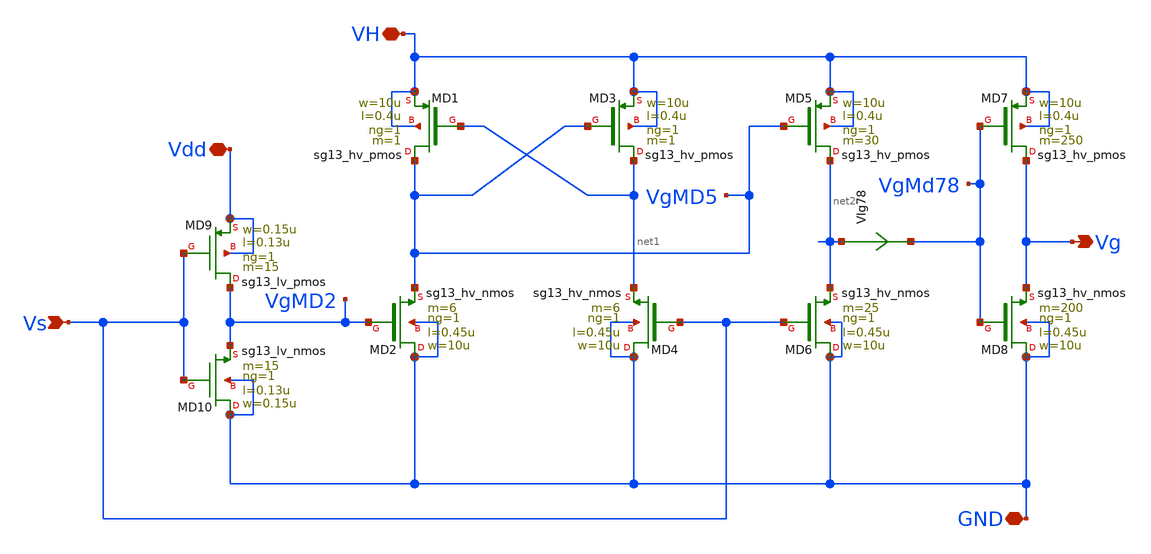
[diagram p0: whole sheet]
** sch_path: ChipUSM_AnalogTrack24/GD/GateDriverV2.sch
**.subckt GateDriverV2 VH Vdd Vs Vg GND
*.iopin VH
*.iopin Vdd
*.ipin Vs
*.opin Vg
*.iopin GND
XMD9 VgMD2 Vs Vdd Vdd sg13_lv_pmos w=0.15u l=0.13u ng=1 m=15 mm_ok=1
XMD10 GND Vs VgMD2 GND sg13_lv_nmos w=0.15u l=0.13u ng=1 m=15 mm_ok=1
XMD1 VgMD5 net1 VH VH sg13_hv_pmos w=10u l=0.4u ng=1 m=1 mm_ok=1
XMD3 net1 VgMD5 VH VH sg13_hv_pmos w=10u l=0.4u ng=1 m=1 mm_ok=1
XMD5 net2 VgMD5 VH VH sg13_hv_pmos w=10u l=0.4u ng=1 m=30 mm_ok=1
XMD7 Vg VgMd78 VH VH sg13_hv_pmos w=10u l=0.4u ng=1 m=250 mm_ok=1
XMD2 GND VgMD2 VgMD5 GND sg13_hv_nmos w=10u l=0.45u ng=1 m=6 mm_ok=1
XMD4 GND Vs net1 GND sg13_hv_nmos w=10u l=0.45u ng=1 m=6 mm_ok=1
XMD6 GND Vs net2 GND sg13_hv_nmos w=10u l=0.45u ng=1 m=25 mm_ok=1
XMD8 GND VgMd78 Vg GND sg13_hv_nmos w=10u l=0.45u ng=1 m=200 mm_ok=1
VIg78 net2 VgMd78 0
.save i(vig78)
**.ends
.end
